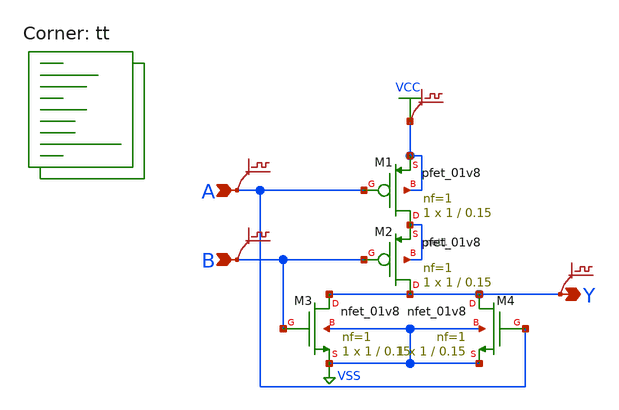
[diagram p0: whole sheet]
** sch_path: elements/or5.sch
**.subckt or5 A B Y
*.ipin A
*.ipin B
*.opin Y
XM1 net1 A VCC VCC sky130_fd_pr__pfet_01v8 L=0.15 W=1 nf=1 ad='int((nf+1)/2) * W/nf * 0.29' as='int((nf+2)/2) * W/nf * 0.29'
+ pd='2*int((nf+1)/2) * (W/nf + 0.29)' ps='2*int((nf+2)/2) * (W/nf + 0.29)' nrd='0.29 / W' nrs='0.29 / W'
+ sa=0 sb=0 sd=0 mult=1 m=1
XM2 Y B net1 net1 sky130_fd_pr__pfet_01v8 L=0.15 W=1 nf=1 ad='int((nf+1)/2) * W/nf * 0.29' as='int((nf+2)/2) * W/nf * 0.29'
+ pd='2*int((nf+1)/2) * (W/nf + 0.29)' ps='2*int((nf+2)/2) * (W/nf + 0.29)' nrd='0.29 / W' nrs='0.29 / W'
+ sa=0 sb=0 sd=0 mult=1 m=1
XM3 Y B VSS VSS sky130_fd_pr__nfet_01v8 L=0.15 W=1 nf=1 ad='int((1 + 1)/2) * 1 / 1 * 0.29' as='int((1 + 2)/2) * 1 / 1 * 0.29'
+ pd='2*int((1 + 1)/2) * (1 / 1 + 0.29)' ps='2*int((1 + 2)/2) * (1 / 1 + 0.29)' nrd='0.29 / 1 ' nrs='0.29 / 1 '
+ sa=0 sb=0 sd=0 mult=1 m=1
XM4 Y A VSS VSS sky130_fd_pr__nfet_01v8 L=0.15 W=1 nf=1 ad='int((1 + 1)/2) * 1 / 1 * 0.29' as='int((1 + 2)/2) * 1 / 1 * 0.29'
+ pd='2*int((1 + 1)/2) * (1 / 1 + 0.29)' ps='2*int((1 + 2)/2) * (1 / 1 + 0.29)' nrd='0.29 / 1 ' nrs='0.29 / 1 '
+ sa=0 sb=0 sd=0 mult=1 m=1
.save v(vcc)
.save v(a)
.save v(b)
.save v(y)
**** begin user architecture code
.lib $::SKYWATER_MODELS/sky130.lib.spice tt

.include $::SKYWATER_STDCELLS/sky130_fd_sc_hd.spice




*.option method=gear
.param VCC=1.8

.include stimuli_or5.cir
.control
* save all
tran 0.1n 10n uic
write or5.raw
acct
rusage
.endc



**** end user architecture code
**.ends
.GLOBAL VCC
.GLOBAL VSS
.end
